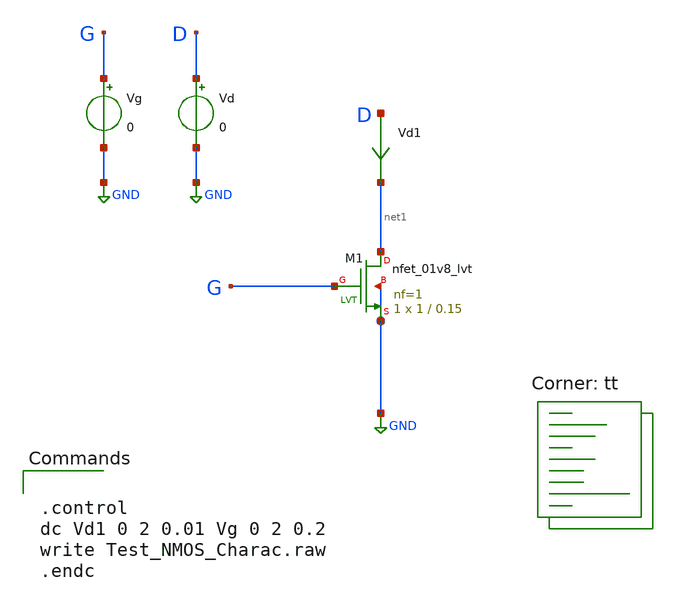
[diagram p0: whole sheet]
** sch_path: XSCHEM_DESIGNS/Test_NMOS_Charac_xyce.sch
**.subckt Test_NMOS_Charac_xyce
Vg G GND 0
XM1 net1 G GND GND sky130_fd_pr__nfet_01v8_lvt L=0.15 W=1 nf=1 ad='int((1 + 1)/2) * 1 / 1 * 0.29' as='int((1 + 2)/2) * 1 / 1 * 0.29'
+ pd='2*int((1 + 1)/2) * (1 / 1 + 0.29)' ps='2*int((1 + 2)/2) * (1 / 1 + 0.29)' nrd='0.29 / 1 ' nrs='0.29 / 1 '
+ sa=0 sb=0 sd=0 mult=1 m=1
Vd1 D net1 0
.save i(vd1)
Vd D GND 0
**** begin user architecture code
.lib $::SKYWATER_MODELS/sky130.lib.spice tt


.control
dc Vd1 0 2 0.01 Vg 0 2 0.2
write Test_NMOS_Charac.raw
.endc


**** end user architecture code
**.ends
.GLOBAL GND
.end
